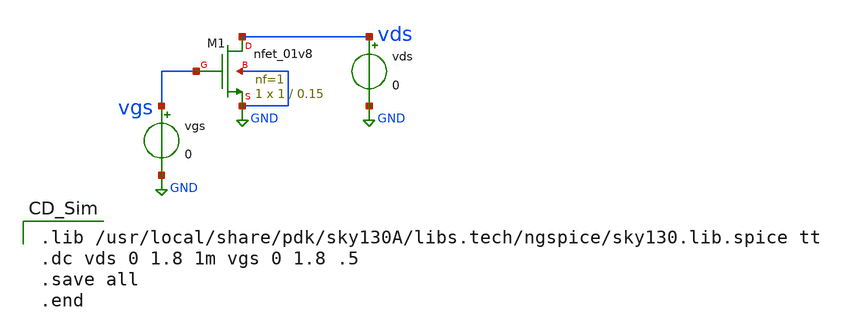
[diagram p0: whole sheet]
** sch_path: working_dir/nfet_test.sch
**.subckt nfet_test
vgs vgs GND 0
XM1 vds vgs GND GND sky130_fd_pr__nfet_01v8 L=0.15 W=1 nf=1 ad='int((nf+1)/2) * W/nf * 0.29' as='int((nf+2)/2) * W/nf * 0.29'
+ pd='2*int((nf+1)/2) * (W/nf + 0.29)' ps='2*int((nf+2)/2) * (W/nf + 0.29)' nrd='0.29 / W' nrs='0.29 / W'
+ sa=0 sb=0 sd=0 mult=1 m=1
vds vds GND 0
**** begin user architecture code

.lib /usr/local/share/pdk/sky130A/libs.tech/ngspice/sky130.lib.spice tt
.dc vds 0 1.8 1m vgs 0 1.8 .5
.save all
.end

**** end user architecture code
**.ends
.GLOBAL GND
.end
